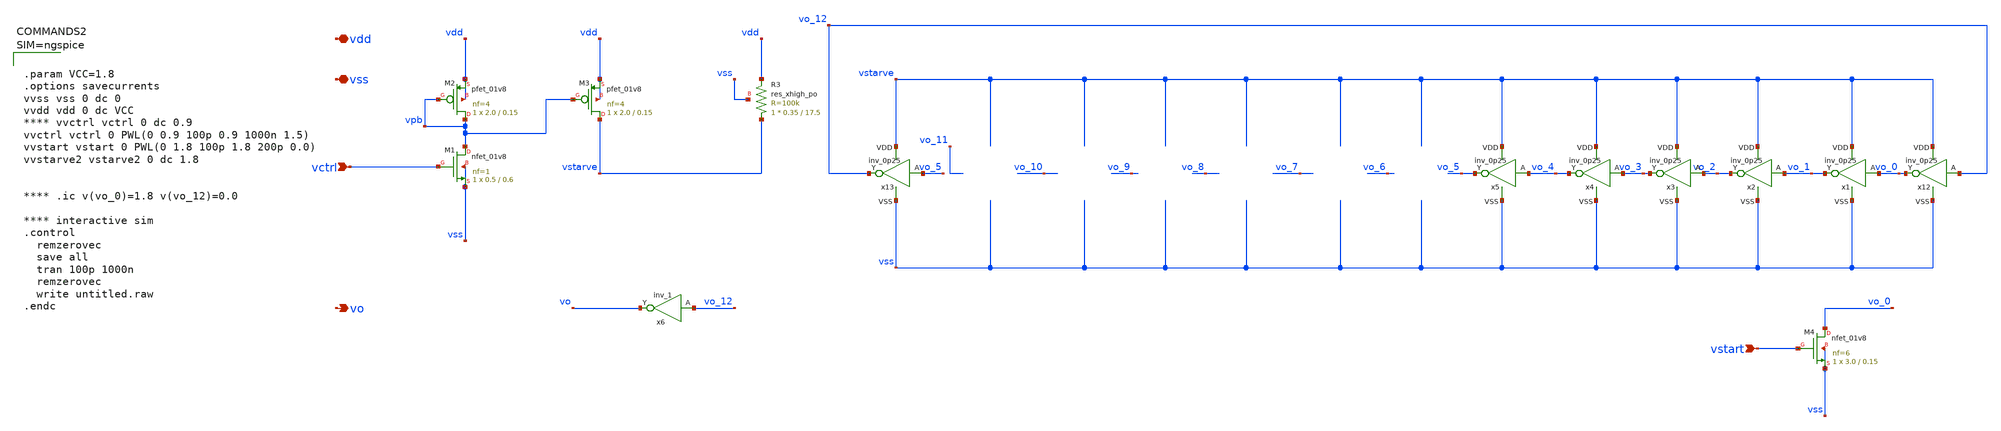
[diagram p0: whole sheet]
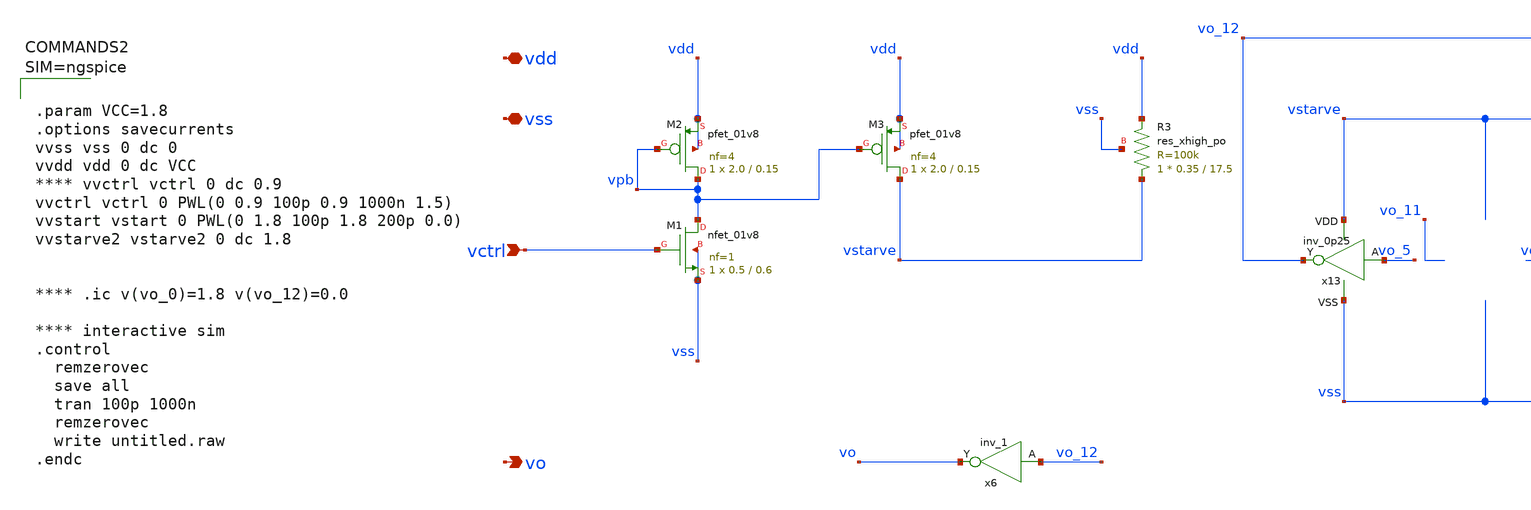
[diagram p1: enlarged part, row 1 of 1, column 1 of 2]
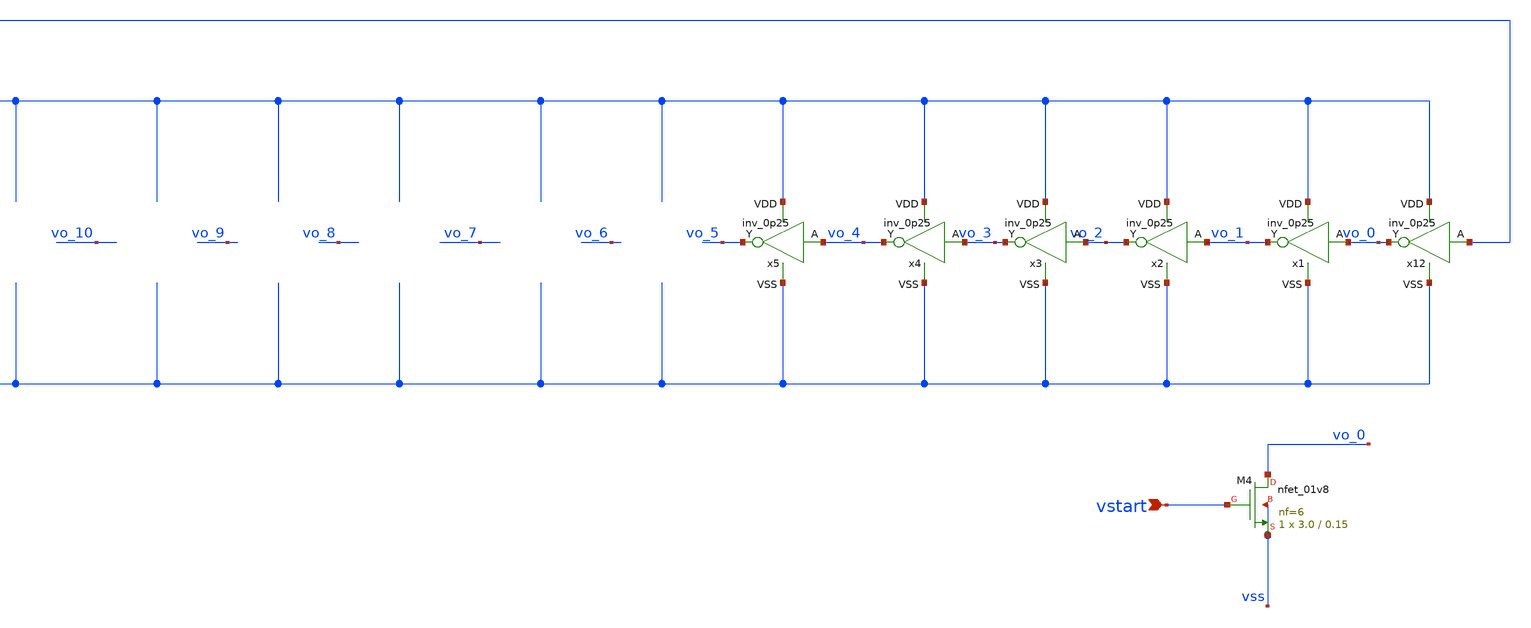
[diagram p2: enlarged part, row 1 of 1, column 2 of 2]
** sch_path: custom_gds/tt_um_mickey_pll/xschem/vcoB.sch
* custom_gds/tt_um_mickey_pll/xschem/inv_0p25.sym:
* Copyright 2022 Stefan Frederik Schippers
* Licensed under the Apache License, Version 2.0 (the "License");
.lib $::SKYWATER_MODELS/sky130.lib.spice tt
.include $::SKYWATER_STDCELLS/sky130_fd_sc_hd.spice

**.subckt vcoB vctrl vdd vss vstart vo
*.ipin vctrl
*.iopin vdd
*.iopin vss
*.ipin vstart
*.opin vo
XM1 vpb vctrl vss vss sky130_fd_pr__nfet_01v8 L=0.6 W=0.5 nf=1 ad='int((nf+1)/2) * W/nf * 0.29' as='int((nf+2)/2) * W/nf * 0.29'
+ pd='2*int((nf+1)/2) * (W/nf + 0.29)' ps='2*int((nf+2)/2) * (W/nf + 0.29)' nrd='0.29 / W' nrs='0.29 / W'
+ sa=0 sb=0 sd=0 mult=1 m=1
XM2 vpb vpb vdd vdd sky130_fd_pr__pfet_01v8 L=0.15 W=2.0 nf=4 ad='int((nf+1)/2) * W/nf * 0.29' as='int((nf+2)/2) * W/nf * 0.29'
+ pd='2*int((nf+1)/2) * (W/nf + 0.29)' ps='2*int((nf+2)/2) * (W/nf + 0.29)' nrd='0.29 / W' nrs='0.29 / W'
+ sa=0 sb=0 sd=0 mult=1 m=1
x13 vo_5 vo_12 vstarve vss inv_0p25
XM3 vstarve vpb vdd vdd sky130_fd_pr__pfet_01v8 L=0.15 W=2.0 nf=4 ad='int((nf+1)/2) * W/nf * 0.29' as='int((nf+2)/2) * W/nf * 0.29'
+ pd='2*int((nf+1)/2) * (W/nf + 0.29)' ps='2*int((nf+2)/2) * (W/nf + 0.29)' nrd='0.29 / W' nrs='0.29 / W'
+ sa=0 sb=0 sd=0 mult=1 m=1
XM4 vo_0 vstart vss vss sky130_fd_pr__nfet_01v8 L=0.15 W=3.0 nf=6 ad='int((nf+1)/2) * W/nf * 0.29' as='int((nf+2)/2) * W/nf * 0.29'
+ pd='2*int((nf+1)/2) * (W/nf + 0.29)' ps='2*int((nf+2)/2) * (W/nf + 0.29)' nrd='0.29 / W' nrs='0.29 / W'
+ sa=0 sb=0 sd=0 mult=1 m=1
x12 vo_12 vo_0 vstarve vss inv_0p25
x1 vo_0 vo_1 vstarve vss inv_0p25
x2 vo_1 vo_2 vstarve vss inv_0p25
x3 vo_2 vo_3 vstarve vss inv_0p25
x4 vo_3 vo_4 vstarve vss inv_0p25
x5 vo_4 vo_5 vstarve vss inv_0p25
x6 vo_12 vss vss vdd vdd vo sky130_fd_sc_hd__inv_1
XR3 vstarve vdd vss sky130_fd_pr__res_xhigh_po W=0.35 L=17.5 mult=1 m=1
**** begin user architecture code



.param VCC=1.8
.options savecurrents
vvss vss 0 dc 0
vvdd vdd 0 dc VCC
**** vvctrl vctrl 0 dc 0.9
vvctrl vctrl 0 PWL(0 0.9 100p 0.9 1000n 1.5)
vvstart vstart 0 PWL(0 1.8 100p 1.8 200p 0.0)
vvstarve2 vstarve2 0 dc 1.8


**** .ic v(vo_0)=1.8 v(vo_12)=0.0

**** interactive sim
.control
  remzerovec
  save all
  tran 100p 1000n
  remzerovec
  write untitled.raw
.endc



**** end user architecture code
**.ends

* expanding   symbol:  sky130_stdcells/inv_0p25.sym # of pins=5
** sym_path: custom_gds/tt_um_mickey_pll/xschem/inv_0p25.sym
** sch_path: custom_gds/tt_um_mickey_pll/xschem/inv_0p25.sch
.subckt inv_0p25 A Y VDD VSS
*.ipin A
*.iopin VDD
*.iopin VSS
*.opin Y
XM1 Y A VSS VSS sky130_fd_pr__nfet_01v8 L=0.60 W=0.65 nf=1 ad='int((nf+1)/2) * W/nf * 0.29' as='int((nf+2)/2) * W/nf * 0.29'
+ pd='2*int((nf+1)/2) * (W/nf + 0.29)' ps='2*int((nf+2)/2) * (W/nf + 0.29)' nrd='0.29 / W' nrs='0.29 / W'
+ sa=0 sb=0 sd=0 mult=1 m=1
XM2 Y A VDD VDD sky130_fd_pr__pfet_01v8_hvt L=0.60 W=1 nf=1 ad='int((nf+1)/2) * W/nf * 0.29' as='int((nf+2)/2) * W/nf * 0.29'
+ pd='2*int((nf+1)/2) * (W/nf + 0.29)' ps='2*int((nf+2)/2) * (W/nf + 0.29)' nrd='0.29 / W' nrs='0.29 / W'
+ sa=0 sb=0 sd=0 mult=1 m=1
.ends

.end
